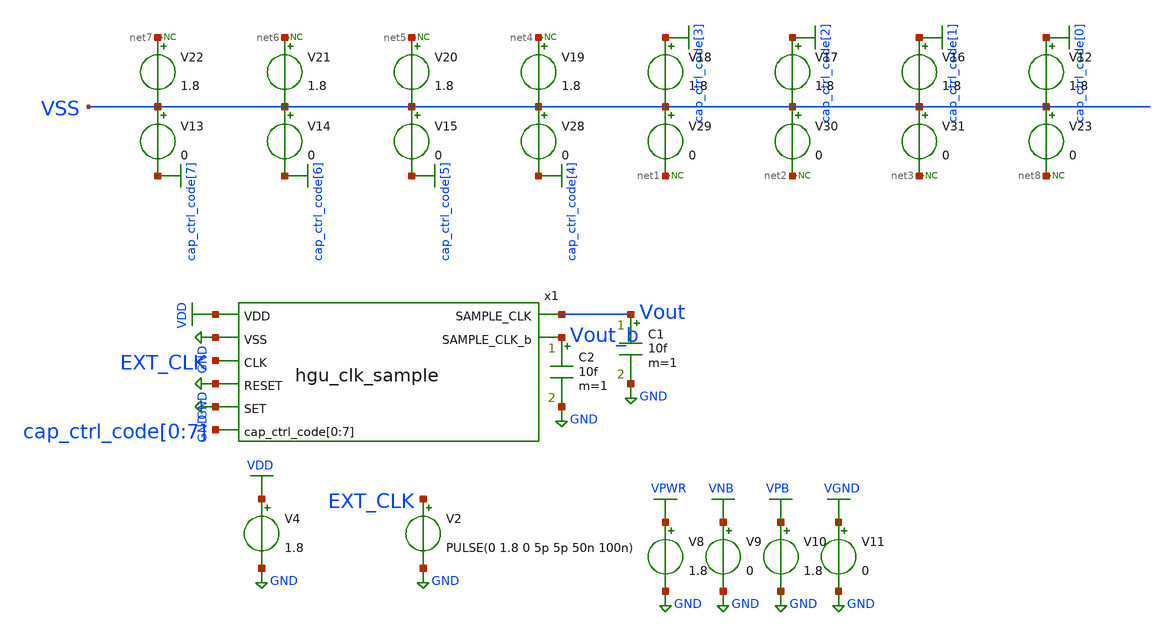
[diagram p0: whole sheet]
** sch_path: hgu/tb/tb_hgu_clk_sample.sch
**.subckt tb_hgu_clk_sample
V2 EXT_CLK GND PULSE(0 1.8 0 5p 5p 50n 100n)
V4 VDD GND 1.8
x1 Vout VDD GND EXT_CLK GND GND Vout_b cap_ctrl_code[0] cap_ctrl_code[1] cap_ctrl_code[2]
+ cap_ctrl_code[3] cap_ctrl_code[4] cap_ctrl_code[5] cap_ctrl_code[6] cap_ctrl_code[7] hgu_clk_sample
C1 Vout GND 10f m=1
V8 VPWR GND 1.8
V9 VNB GND 0
V10 VPB GND 1.8
V11 VGND GND 0
V12 cap_ctrl_code[0] VSS 1.8
V13 VSS cap_ctrl_code[7] 0
V14 VSS cap_ctrl_code[6] 0
V15 VSS cap_ctrl_code[5] 0
V28 VSS cap_ctrl_code[4] 0
V29 VSS net1 0
V30 VSS net2 0
V31 VSS net3 0
V16 cap_ctrl_code[1] VSS 1.8
V17 cap_ctrl_code[2] VSS 1.8
V18 cap_ctrl_code[3] VSS 1.8
V19 net4 VSS 1.8
V20 net5 VSS 1.8
V21 net6 VSS 1.8
V22 net7 VSS 1.8
V23 VSS net8 0
* noconn #net7
* noconn #net6
* noconn #net5
* noconn #net4
* noconn #net1
* noconn #net2
* noconn #net3
* noconn #net8
C2 Vout_b GND 10f m=1
**** begin user architecture code



.lib /foss/pdks/sky130A/libs.tech/ngspice/sky130.lib.spice ff
.include /foss/pdks/sky130A/libs.ref/sky130_fd_sc_hd/spice/sky130_fd_sc_hd.spice


.tran 10ps 200ns

.control
	option temp = 0
	let vdd_act = 1.98

	alter V1 vdd_act

	run
	plot V(Vout) V(Vout_b) V(EXT_CLK)+2

	let l_vdd = vdd_act * 0.2
        let h_vdd = vdd_act * 0.8
        let m_vdd = vdd_act * 0.5
        meas tran rising_s find time when V(Vout)=l_vdd RISE=1 TD=90n
        meas tran rising_e find time when V(Vout)=h_vdd RISE=1 TD=90n
        let rising_time = rising_e-rising_s
        meas tran falling_s find time when V(Vout)=h_vdd FALL=1 TD=90n
        meas tran falling_e find time when V(Vout)=l_vdd FALL=1 TD=90n
        let falling_time = falling_e-falling_s
        meas tran IN find time when V(ext_clk)=m_vdd RISE=1 TD=90n
        meas tran OUT find time when V(Vout)=m_vdd RISE=1 TD=90n
        let rising_delay = OUT-IN

	meas tran IN find time when V(Vout)=m_vdd RISE=1 TD=90n
        meas tran OUT find time when V(Vout)=m_vdd FALL=1 TD=90n
        let on_time = OUT-IN

	print rising_time falling_time rising_delay on_time
.endc
.save all



**** end user architecture code
**.ends
.GLOBAL GND
.GLOBAL VDD
.GLOBAL VGND
.GLOBAL VNB
.GLOBAL VPB
.GLOBAL VPWR
.GLOBAL cap_ctrl_code[7]
.GLOBAL cap_ctrl_code[6]
.GLOBAL cap_ctrl_code[5]
.GLOBAL cap_ctrl_code[4]
.GLOBAL cap_ctrl_code[3]
.GLOBAL cap_ctrl_code[2]
.GLOBAL cap_ctrl_code[1]
.GLOBAL cap_ctrl_code[0]
.end
